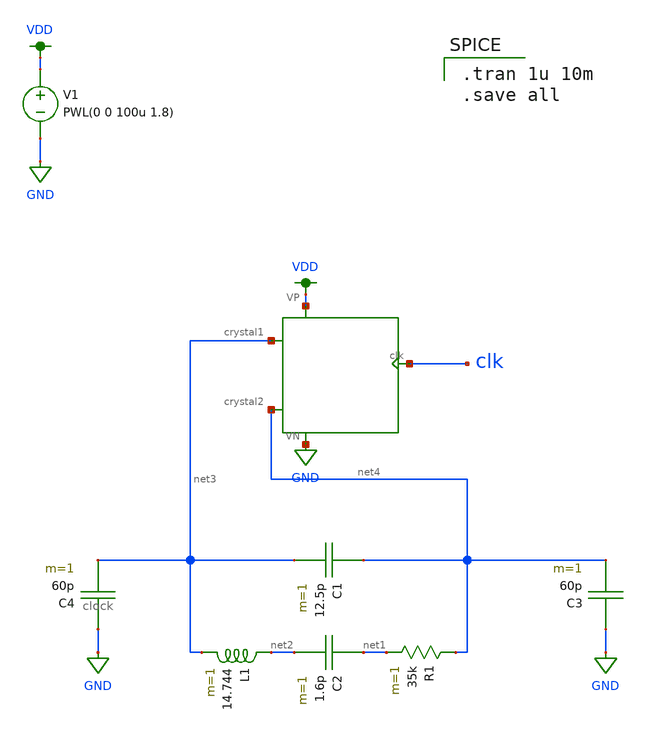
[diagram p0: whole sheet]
** sch_path: analog/osc.sch
**.subckt osc
C1 net4 net3 12.5p m=1
L1 net2 net3 14.744 m=1
C2 net1 net2 1.6p m=1
R1 net4 net1 35k m=1
V1 VDD GND PWL(0 0 100u 1.8)
C3 GND net4 60p m=1
C4 GND net3 60p m=1
X1 net3 net4 clk VDD GND clock
**** begin user architecture code

.tran 1u 10m
.save all


.option wnflag=1
.param MC_SWITCH=0.0
.lib ~/skywater/skywater-pdk/libraries/sky130_fd_pr_ngspice/latest/models/sky130.lib.spice tt

**** end user architecture code
**.ends
.GLOBAL VDD
.GLOBAL GND
.end
